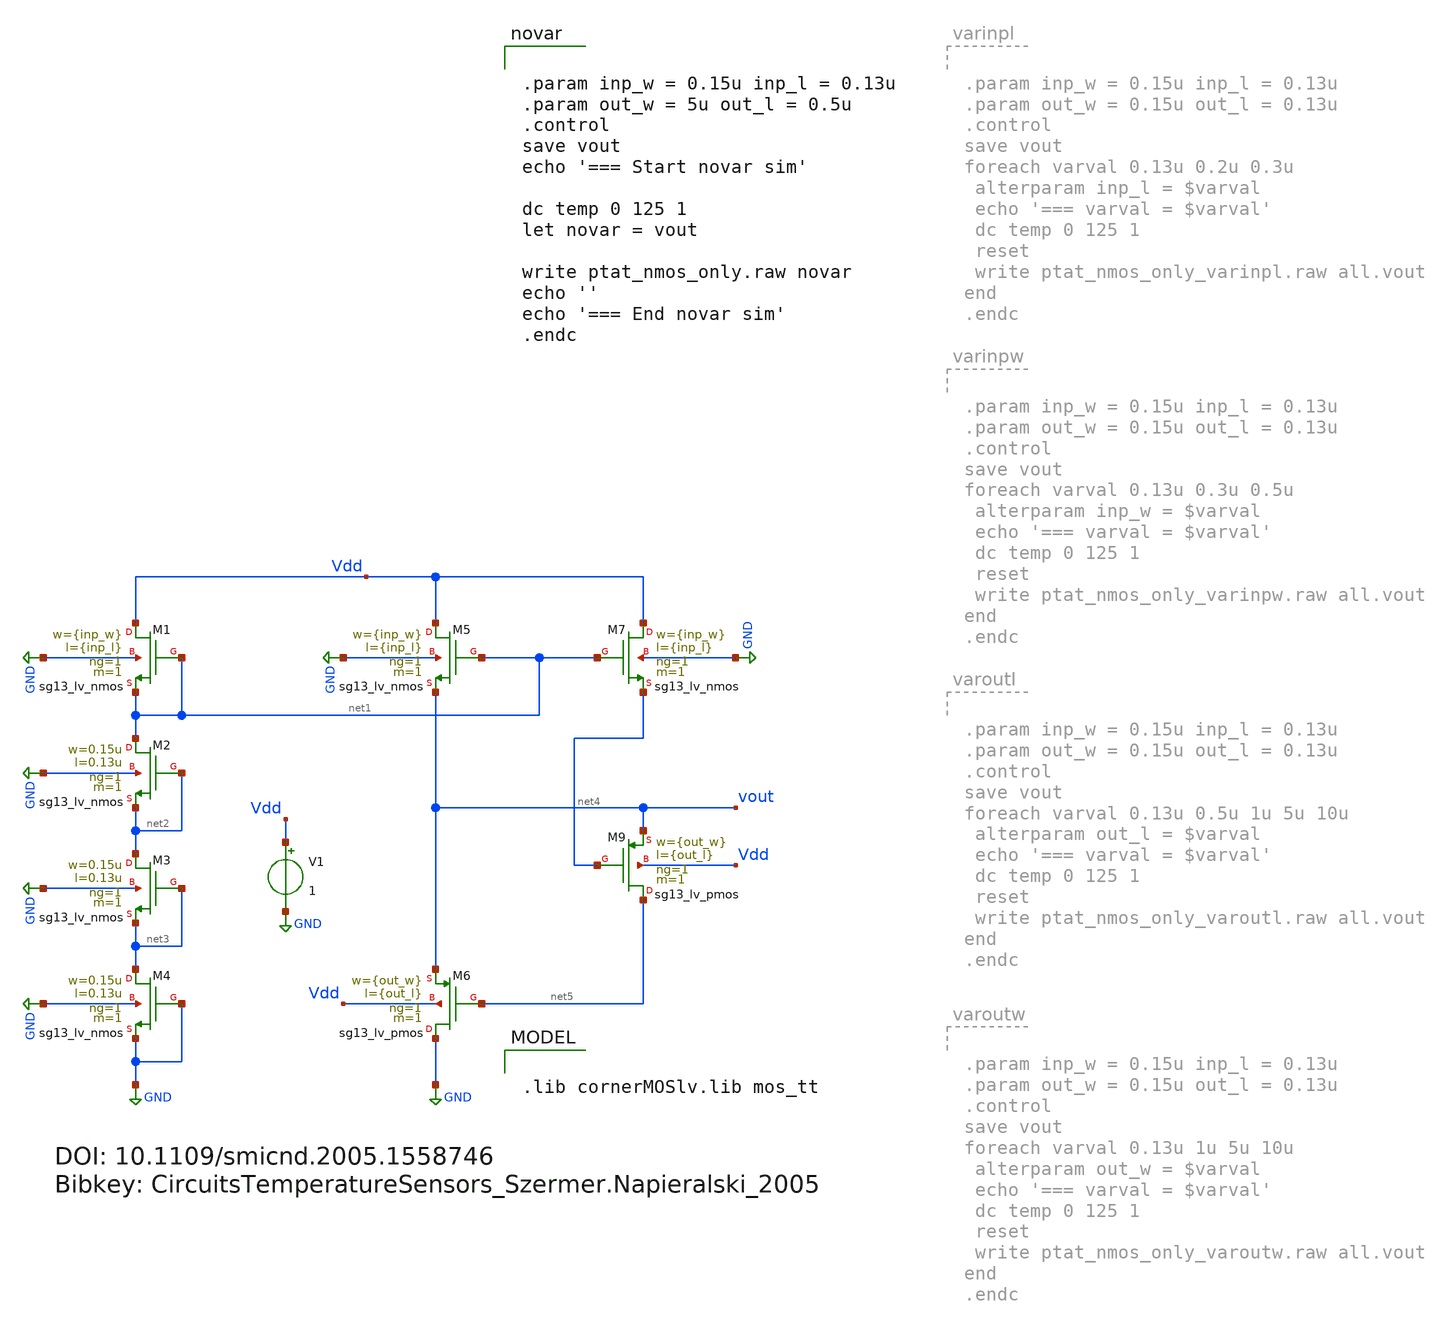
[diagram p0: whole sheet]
** sch_path: TempSensor/design_data/xschem/ptat_nmos_only.sch
**.subckt ptat_nmos_only
XM1 Vdd net1 net1 GND sg13_lv_nmos w={inp_w} l={inp_l} ng=1 m=1 mm_ok=1
XM2 net1 net2 net2 GND sg13_lv_nmos w=0.15u l=0.13u ng=1 m=1 mm_ok=1
XM3 net2 net3 net3 GND sg13_lv_nmos w=0.15u l=0.13u ng=1 m=1 mm_ok=1
XM4 net3 GND GND GND sg13_lv_nmos w=0.15u l=0.13u ng=1 m=1 mm_ok=1
XM5 Vdd net1 vout GND sg13_lv_nmos w={inp_w} l={inp_l} ng=1 m=1 mm_ok=1
XM7 Vdd net1 net4 GND sg13_lv_nmos w={inp_w} l={inp_l} ng=1 m=1 mm_ok=1
V1 Vdd GND 1
XM9 net5 net4 vout Vdd sg13_lv_pmos w={out_w} l={out_l} ng=1 m=1 mm_ok=1
XM6 GND net5 vout Vdd sg13_lv_pmos w={out_w} l={out_l} ng=1 m=1 mm_ok=1
**** begin user architecture code

.lib cornerMOSlv.lib mos_tt



.param inp_w = 0.15u inp_l = 0.13u
.param out_w = 5u out_l = 0.5u
.control
save vout
echo '=== Start novar sim'

dc temp 0 125 1
let novar = vout

write ptat_nmos_only.raw novar
echo ''
echo '=== End novar sim'
.endc


**** end user architecture code
**.ends
.GLOBAL GND
.end
